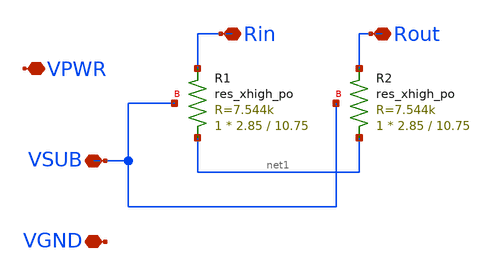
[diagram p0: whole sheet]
** sch_path: xschem/xschem/analog_stdcells/skywater_asc_res_xhigh_po_2p85_2.sch
**.subckt skywater_asc_res_xhigh_po_2p85_2 Rin Rout VPWR VSUB VGND
*.iopin Rin
*.iopin Rout
*.iopin VPWR
*.iopin VSUB
*.iopin VGND
XR1 net1 Rin VSUB sky130_fd_pr__res_xhigh_po W=2.85 L=10.75 mult=1 m=1
XR2 net1 Rout VSUB sky130_fd_pr__res_xhigh_po W=2.85 L=10.75 mult=1 m=1
**.ends
.end
